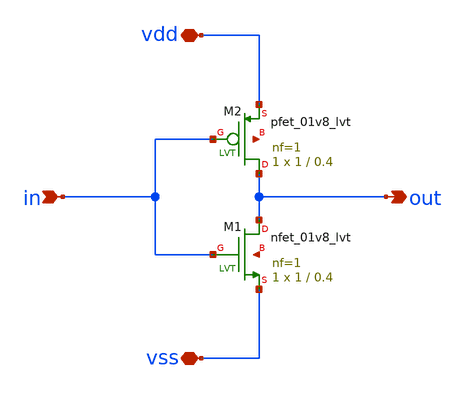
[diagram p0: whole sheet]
** sch_path: xschem/sub/inv_lvt.sch
**.subckt inv_lvt out in vss vdd
*.opin out
*.ipin in
*.iopin vss
*.iopin vdd
XM1 out in vss net1 sky130_fd_pr__nfet_01v8_lvt L=0.4 W=1 nf=1 ad='int((nf+1)/2) * W/nf * 0.29' as='int((nf+2)/2) * W/nf * 0.29'
+ pd='2*int((nf+1)/2) * (W/nf + 0.29)' ps='2*int((nf+2)/2) * (W/nf + 0.29)' nrd='0.29 / W' nrs='0.29 / W'
+ sa=0 sb=0 sd=0 mult=1 m=1
XM2 out in vdd net2 sky130_fd_pr__pfet_01v8_lvt L=0.4 W=1 nf=1 ad='int((nf+1)/2) * W/nf * 0.29' as='int((nf+2)/2) * W/nf * 0.29'
+ pd='2*int((nf+1)/2) * (W/nf + 0.29)' ps='2*int((nf+2)/2) * (W/nf + 0.29)' nrd='0.29 / W' nrs='0.29 / W'
+ sa=0 sb=0 sd=0 mult=1 m=1
**.ends
.end
